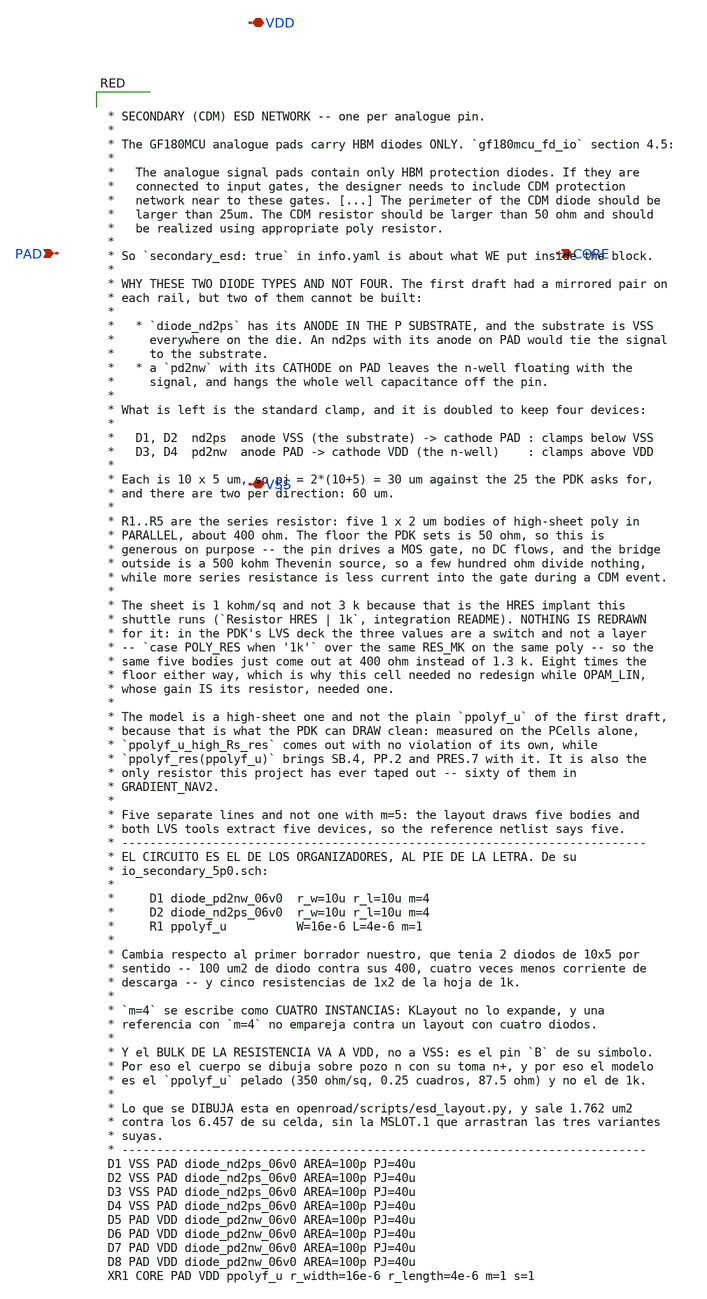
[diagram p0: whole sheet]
** sch_path: FINAL/XSCHEM_v2/ESD_CDM.sch
**.subckt ESD_CDM PAD CORE VDD VSS
*.ipin PAD
*.opin CORE
*.iopin VDD
*.iopin VSS
**** begin user architecture code


* SECONDARY (CDM) ESD NETWORK -- one per analogue pin.
*
* The GF180MCU analogue pads carry HBM diodes ONLY. `gf180mcu_fd_io` section 4.5:
*
*   The analogue signal pads contain only HBM protection diodes. If they are
*   connected to input gates, the designer needs to include CDM protection
*   network near to these gates. [...] The perimeter of the CDM diode should be
*   larger than 25um. The CDM resistor should be larger than 50 ohm and should
*   be realized using appropriate poly resistor.
*
* So `secondary_esd: true` in info.yaml is about what WE put inside the block.
*
* WHY THESE TWO DIODE TYPES AND NOT FOUR. The first draft had a mirrored pair on
* each rail, but two of them cannot be built:
*
*   * `diode_nd2ps` has its ANODE IN THE P SUBSTRATE, and the substrate is VSS
*     everywhere on the die. An nd2ps with its anode on PAD would tie the signal
*     to the substrate.
*   * a `pd2nw` with its CATHODE on PAD leaves the n-well floating with the
*     signal, and hangs the whole well capacitance off the pin.
*
* What is left is the standard clamp, and it is doubled to keep four devices:
*
*   D1, D2  nd2ps  anode VSS (the substrate) -> cathode PAD : clamps below VSS
*   D3, D4  pd2nw  anode PAD -> cathode VDD (the n-well)    : clamps above VDD
*
* Each is 10 x 5 um, so pj = 2*(10+5) = 30 um against the 25 the PDK asks for,
* and there are two per direction: 60 um.
*
* R1..R5 are the series resistor: five 1 x 2 um bodies of high-sheet poly in
* PARALLEL, about 400 ohm. The floor the PDK sets is 50 ohm, so this is
* generous on purpose -- the pin drives a MOS gate, no DC flows, and the bridge
* outside is a 500 kohm Thevenin source, so a few hundred ohm divide nothing,
* while more series resistance is less current into the gate during a CDM event.
*
* The sheet is 1 kohm/sq and not 3 k because that is the HRES implant this
* shuttle runs (`Resistor HRES | 1k`, integration README). NOTHING IS REDRAWN
* for it: in the PDK's LVS deck the three values are a switch and not a layer
* -- `case POLY_RES when '1k'` over the same RES_MK on the same poly -- so the
* same five bodies just come out at 400 ohm instead of 1.3 k. Eight times the
* floor either way, which is why this cell needed no redesign while OPAM_LIN,
* whose gain IS its resistor, needed one.
*
* The model is a high-sheet one and not the plain `ppolyf_u` of the first draft,
* because that is what the PDK can DRAW clean: measured on the PCells alone,
* `ppolyf_u_high_Rs_res` comes out with no violation of its own, while
* `ppolyf_res(ppolyf_u)` brings SB.4, PP.2 and PRES.7 with it. It is also the
* only resistor this project has ever taped out -- sixty of them in
* GRADIENT_NAV2.
*
* Five separate lines and not one with m=5: the layout draws five bodies and
* both LVS tools extract five devices, so the reference netlist says five.
* ---------------------------------------------------------------------------
* EL CIRCUITO ES EL DE LOS ORGANIZADORES, AL PIE DE LA LETRA. De su
* io_secondary_5p0.sch:
*
*     D1 diode_pd2nw_06v0  r_w=10u r_l=10u m=4
*     D2 diode_nd2ps_06v0  r_w=10u r_l=10u m=4
*     R1 ppolyf_u          W=16e-6 L=4e-6 m=1
*
* Cambia respecto al primer borrador nuestro, que tenia 2 diodos de 10x5 por
* sentido -- 100 um2 de diodo contra sus 400, cuatro veces menos corriente de
* descarga -- y cinco resistencias de 1x2 de la hoja de 1k.
*
* `m=4` se escribe como CUATRO INSTANCIAS: KLayout no lo expande, y una
* referencia con `m=4` no empareja contra un layout con cuatro diodos.
*
* Y el BULK DE LA RESISTENCIA VA A VDD, no a VSS: es el pin `B` de su simbolo.
* Por eso el cuerpo se dibuja sobre pozo n con su toma n+, y por eso el modelo
* es el `ppolyf_u` pelado (350 ohm/sq, 0.25 cuadros, 87.5 ohm) y no el de 1k.
*
* Lo que se DIBUJA esta en openroad/scripts/esd_layout.py, y sale 1.762 um2
* contra los 6.457 de su celda, sin la MSLOT.1 que arrastran las tres variantes
* suyas.
* ---------------------------------------------------------------------------
D1 VSS PAD diode_nd2ps_06v0 AREA=100p PJ=40u
D2 VSS PAD diode_nd2ps_06v0 AREA=100p PJ=40u
D3 VSS PAD diode_nd2ps_06v0 AREA=100p PJ=40u
D4 VSS PAD diode_nd2ps_06v0 AREA=100p PJ=40u
D5 PAD VDD diode_pd2nw_06v0 AREA=100p PJ=40u
D6 PAD VDD diode_pd2nw_06v0 AREA=100p PJ=40u
D7 PAD VDD diode_pd2nw_06v0 AREA=100p PJ=40u
D8 PAD VDD diode_pd2nw_06v0 AREA=100p PJ=40u
XR1 CORE PAD VDD ppolyf_u r_width=16e-6 r_length=4e-6 m=1 s=1


**** end user architecture code
**.ends
.end
